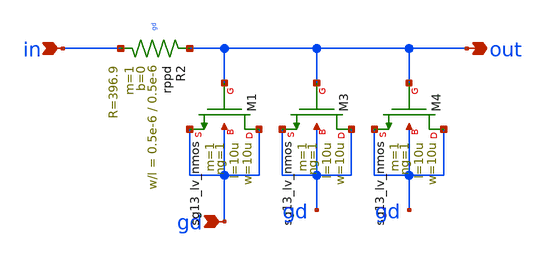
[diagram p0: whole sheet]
** sch_path: schematics/misc/RC_filter.sch
**.subckt RC_filter in out gd
*.ipin in
*.opin out
*.ipin gd
XM1 gd out gd gd sg13_lv_nmos w=10u l=10u ng=1 m=1 mm_ok=1
XM3 gd out gd gd sg13_lv_nmos w=10u l=10u ng=1 m=1 mm_ok=1
XM4 gd out gd gd sg13_lv_nmos w=10u l=10u ng=1 m=1 mm_ok=1
XR2 out in gd rppd w=0.5e-6 l=0.5e-6 m=1 b=0 mm_ok=1
**.ends
.end
